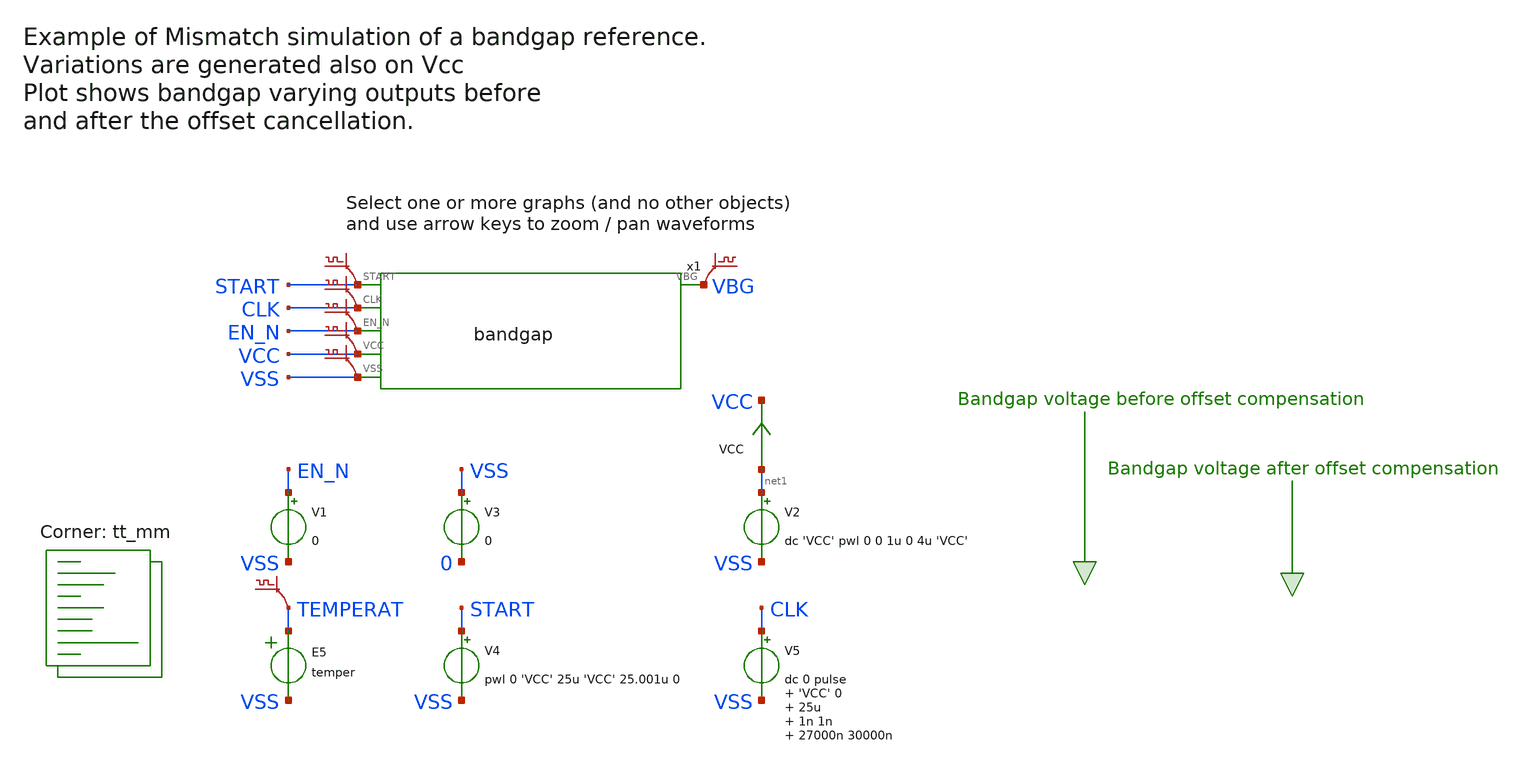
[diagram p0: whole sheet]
** sch_path: sky130A/xschem_libs/sky130_tests/tb_bandgap/schematic/tb_bandgap.sch
* Copyright 2021 Stefan Frederik Schippers
* Licensed under the Apache License, Version 2.0 (the "License");
* you may not use this file except in compliance with the License.
* You may obtain a copy of the License at
* https://www.apache.org/licenses/LICENSE-2.0
* Unless required by applicable law or agreed to in writing, software
* distributed under the License is distributed on an "AS IS" BASIS,
* WITHOUT WARRANTIES OR CONDITIONS OF ANY KIND, either express or implied.
* See the License for the specific language governing permissions and
* limitations under the License.
**.subckt tb_bandgap
x1 START CLK EN_N VBG VCC VSS bandgap
V1 EN_N VSS 0
V2 net1 VSS dc 'VCC' pwl 0 0 1u 0 4u 'VCC'
V3 VSS 0 0
E5 TEMPERAT VSS VOL=' temper '
V4 START VSS pwl 0 'VCC' 25u 'VCC' 25.001u 0
V5 CLK VSS dc 0 pulse 'VCC' 0 25u 1n 1n 27000n 30000n
.save v(vbg)
.save v(start)
.save v(clk)
.save v(en_n)
.save v(vcc)
.save v(vss)
.save v(temperat)
VCC net1 VCC 0
.save i(vcc)
**** begin user architecture code


* this experimental option enables mos model bin
* selection based on W/NF instead of W
* .options wnflag=1 XMU=0.49 METHOD=GEAR ITL4=100 CHGTOL=1e-15 TRTOL=1 RELTOL=0.0001 VNTOL=0.1u
.options method=gear
.param ABSVAR=0.03
.param VCCGAUSS=agauss(1.8, 'ABSVAR', 1)
.param VCC=VCCGAUSS
* .param VCC=1.8
** variation marameters:
* .options savecurrents
.control
  setseed 12
  reset
  op
  write tb_bandgap.raw
  set appendwrite
  let run=1
  dowhile run <= 5
    if run > 1
      reset
    end
    * save all
    if run % 3 = 1
      set temp=-40
    end
    if run % 3 = 2
      set temp=27
    end
    if run % 3 = 0
      set temp=125
    end
    echo "Run=$&run, Temp=$temp"
    tran 10n 200u
    write tb_bandgap.raw
    let run = run + 1
  end
  quit 0
.endc


.lib $::SKYWATER_MODELS/sky130.lib.spice tt_mm
**** end user architecture code
**.ends
.end
